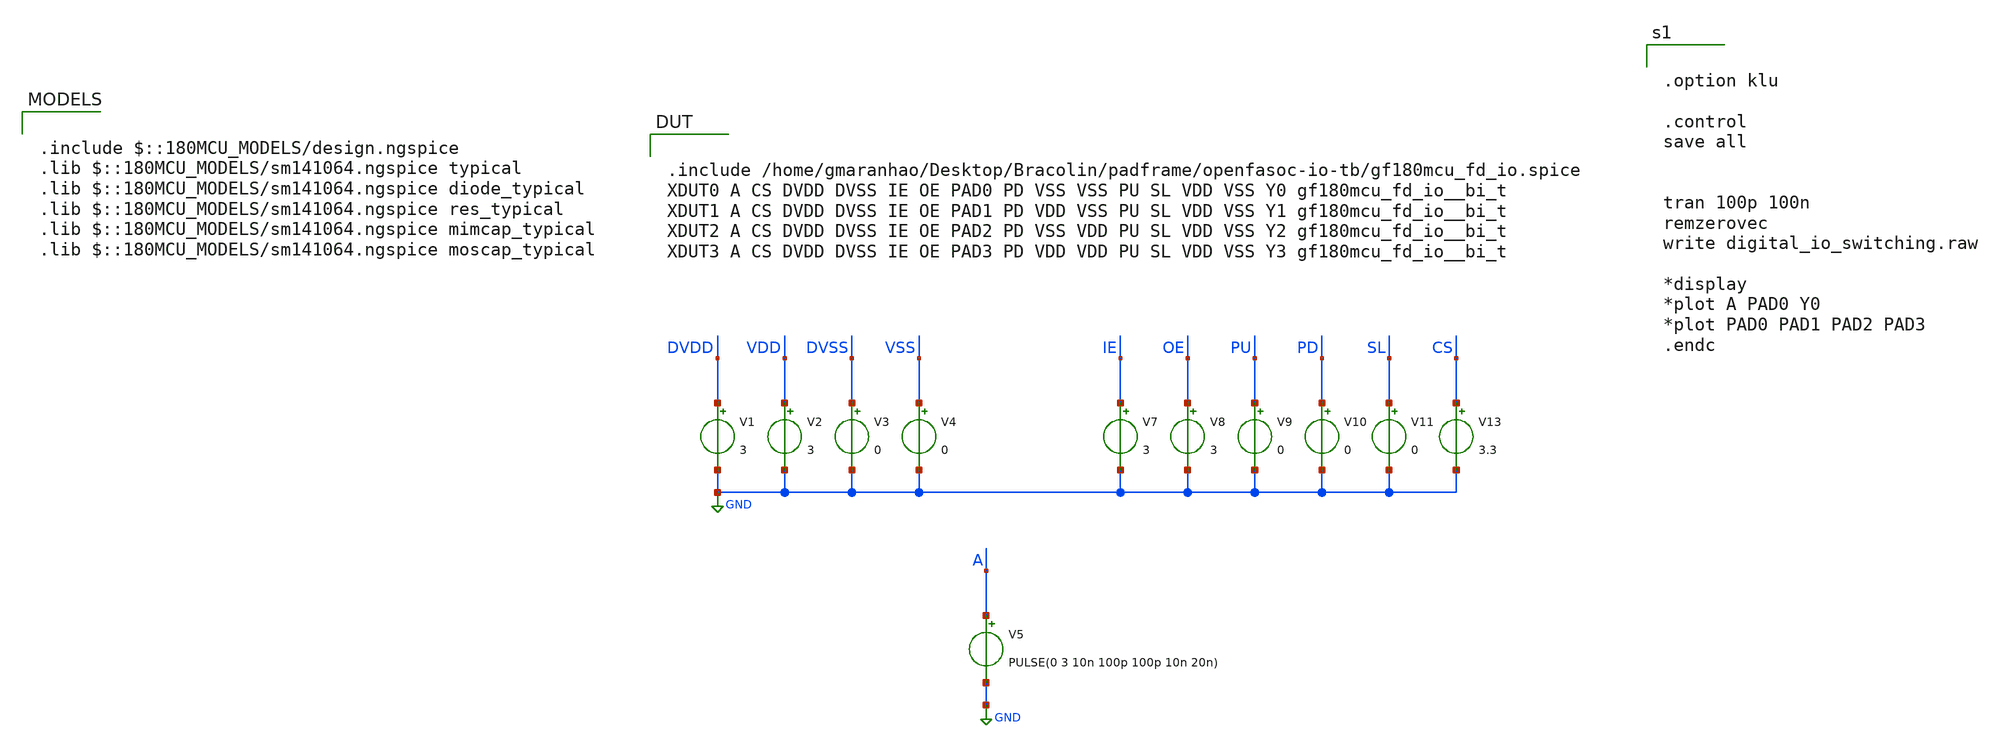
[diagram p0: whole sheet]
** sch_path: padframe/openfasoc-io-tb/digital_io_switching.sch
**.subckt digital_io_switching
V1 DVDD GND 3
V2 VDD GND 3
V3 DVSS GND 0
V4 VSS GND 0
V5 A GND PULSE(0 3 10n 100p 100p 10n 20n)
V7 IE GND 3
V8 OE GND 3
V9 PU GND 0
V10 PD GND 0
V11 SL GND 0
V13 CS GND 3.3
**** begin user architecture code


.option klu

.control
save all


tran 100p 100n
remzerovec
write digital_io_switching.raw

*display
*plot A PAD0 Y0
*plot PAD0 PAD1 PAD2 PAD3
.endc



.include $::180MCU_MODELS/design.ngspice
.lib $::180MCU_MODELS/sm141064.ngspice typical
.lib $::180MCU_MODELS/sm141064.ngspice diode_typical
.lib $::180MCU_MODELS/sm141064.ngspice res_typical
.lib $::180MCU_MODELS/sm141064.ngspice mimcap_typical
.lib $::180MCU_MODELS/sm141064.ngspice moscap_typical


.include /home/gmaranhao/Desktop/Bracolin/padframe/openfasoc-io-tb/gf180mcu_fd_io.spice
XDUT0 A CS DVDD DVSS IE OE PAD0 PD VSS VSS PU SL VDD VSS Y0 gf180mcu_fd_io__bi_t
XDUT1 A CS DVDD DVSS IE OE PAD1 PD VDD VSS PU SL VDD VSS Y1 gf180mcu_fd_io__bi_t
XDUT2 A CS DVDD DVSS IE OE PAD2 PD VSS VDD PU SL VDD VSS Y2 gf180mcu_fd_io__bi_t
XDUT3 A CS DVDD DVSS IE OE PAD3 PD VDD VDD PU SL VDD VSS Y3 gf180mcu_fd_io__bi_t

**** end user architecture code
**.ends
.GLOBAL GND
.end
